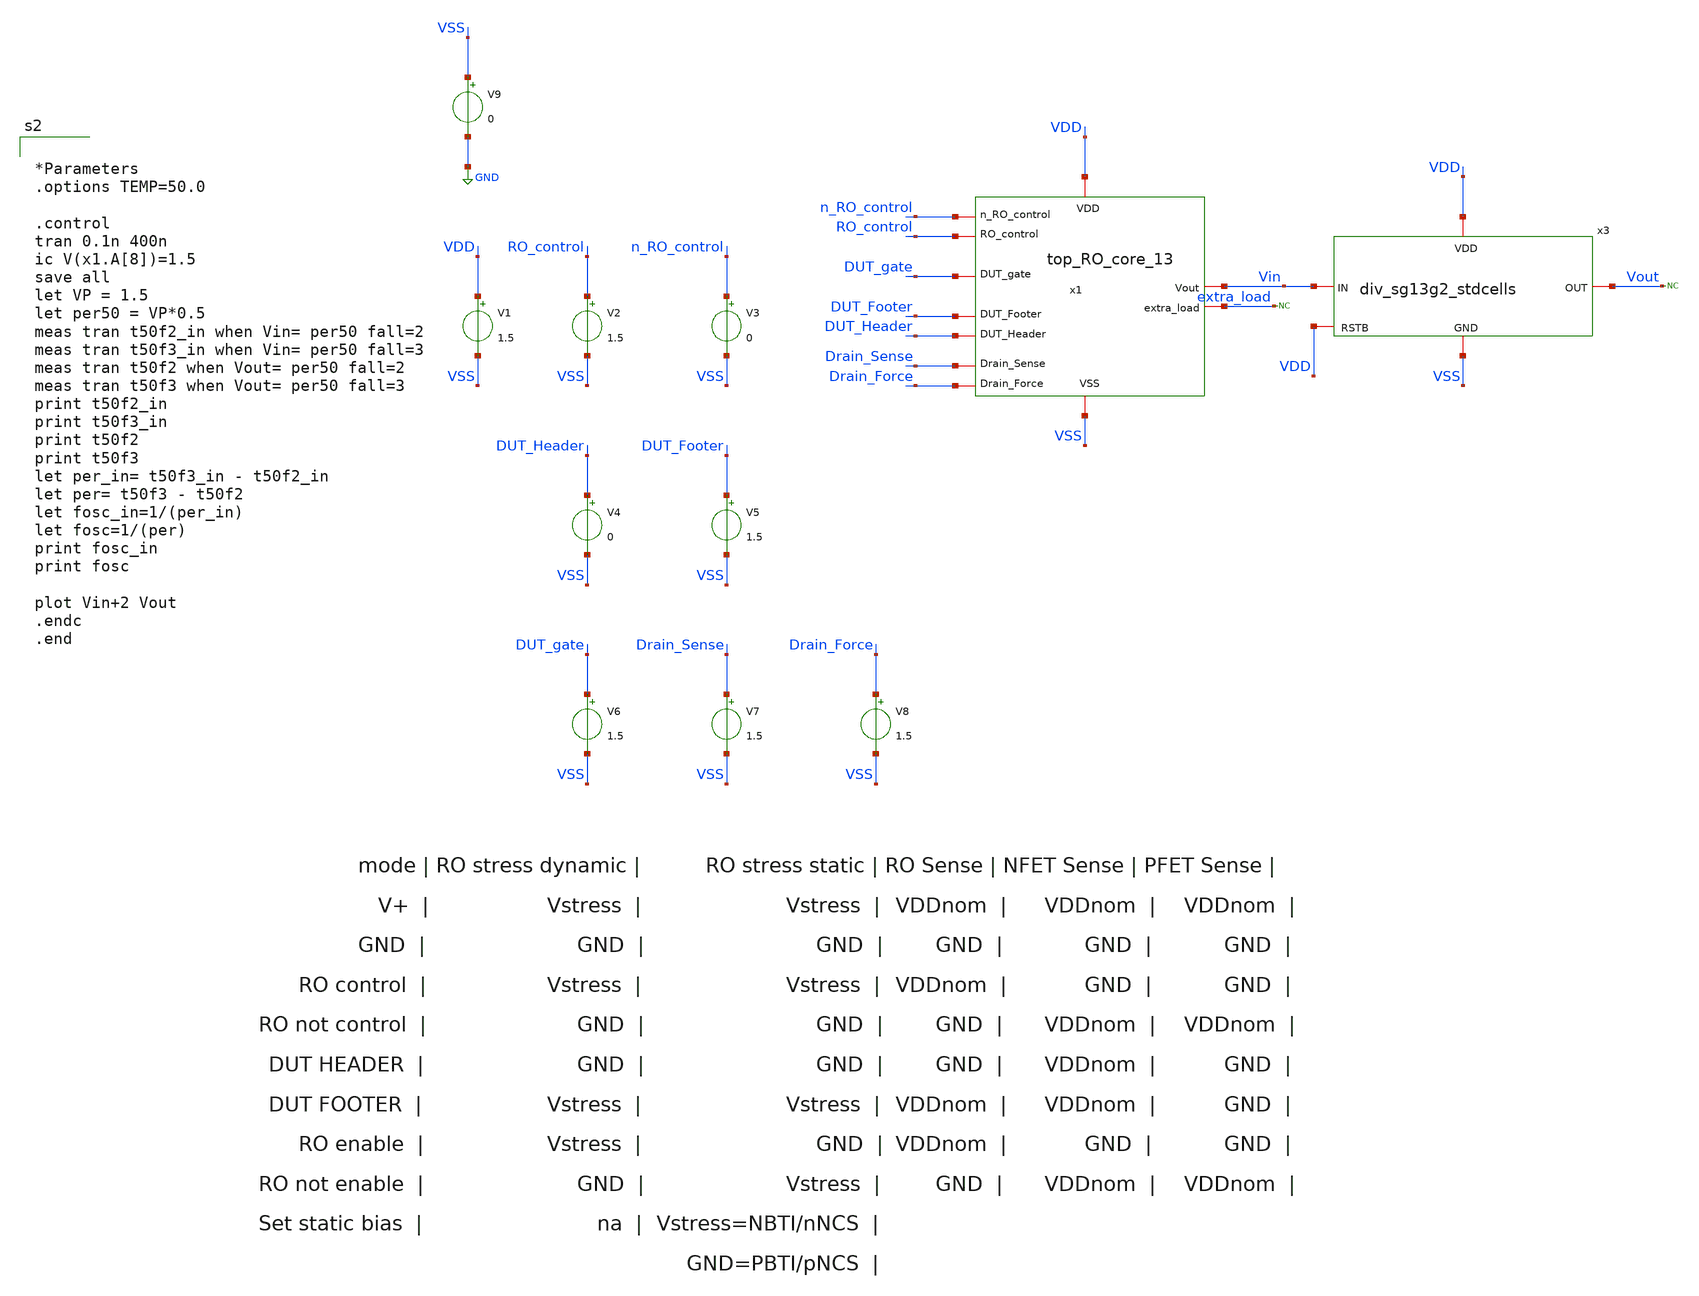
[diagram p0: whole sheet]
** sch_path: unic_cass_wrapper_user_project/ROs_reliability/top_RO_core_13_tb.sch
**.subckt top_RO_core_13_tb
V1 VDD VSS 1.5
V2 RO_control VSS 1.5
V3 n_RO_control VSS 0
V4 DUT_Header VSS 0
V5 DUT_Footer VSS 1.5
* noconn extra_load
* noconn Vout
x1 VDD VSS n_RO_control RO_control DUT_gate Vin DUT_Header DUT_Footer Drain_Force Drain_Sense
+ extra_load top_RO_core_13
V6 DUT_gate VSS 1.5
V7 Drain_Sense VSS 1.5
V8 Drain_Force VSS 1.5
V9 VSS GND 0
x3 VDD Vout Vin VSS VDD div_sg13g2_stdcells
**** begin user architecture code


*Parameters
.options TEMP=50.0

.control
tran 0.1n 400n
ic V(x1.A[8])=1.5
save all
let VP = 1.5
let per50 = VP*0.5
meas tran t50f2_in when Vin= per50 fall=2
meas tran t50f3_in when Vin= per50 fall=3
meas tran t50f2 when Vout= per50 fall=2
meas tran t50f3 when Vout= per50 fall=3
print t50f2_in
print t50f3_in
print t50f2
print t50f3
let per_in= t50f3_in - t50f2_in
let per= t50f3 - t50f2
let fosc_in=1/(per_in)
let fosc=1/(per)
print fosc_in
print fosc

plot Vin+2 Vout
.endc
.end


 .lib cornerMOSlv.lib mos_tt
.include sg13g2_stdcell.spice
.include /home/jsmoya07/Documents/asicone_sg13g2/lib/sg13g2.ckt

**** end user architecture code
**.ends

* expanding   symbol:  top_RO_core_13.sym # of pins=11
** sym_path: unic_cass_wrapper_user_project/ROs_reliability/top_RO_core_13.sym
** sch_path: unic_cass_wrapper_user_project/ROs_reliability/top_RO_core_13.sch
.subckt top_RO_core_13 VDD VSS n_RO_control RO_control DUT_gate Vout DUT_Header DUT_Footer
+ Drain_Force Drain_Sense extra_load
*.iopin VDD
*.iopin VSS
*.iopin n_RO_control
*.iopin RO_control
*.iopin DUT_gate
*.iopin extra_load
*.iopin DUT_Header
*.iopin DUT_Footer
*.iopin Drain_Force
*.iopin Drain_Sense
*.iopin Vout
x1 VDD VSS A[9] A[8] rovcel2
x7 VDD VSS A[9] n_RO_control A_10 RO_control DUT_gate rovcel3
x2 DUT_Header DUT_Footer Drain_Force Drain_Sense RO_control n_RO_control VDD VSS A_10 extra_load
+ rovcel1
x3 VDD VSS extra_load n_RO_control A_12 rovcel4
x4 VDD VSS Vout A_12 rovcel2
x5[1] VDD VSS A[8] A[7] rovcel2
x5[2] VDD VSS A[7] A[6] rovcel2
x5[3] VDD VSS A[6] A[5] rovcel2
x5[4] VDD VSS A[5] A[4] rovcel2
x5[5] VDD VSS A[4] A[3] rovcel2
x5[6] VDD VSS A[3] A[2] rovcel2
x5[7] VDD VSS A[2] A[1] rovcel2
x5[8] VDD VSS A[1] Vout rovcel2
.ends


* expanding   symbol:  /home/jsmoya07/Documents/RO_reliability/xschem/div_sg13g2_stdcells.sym # of
*+ pins=5
** sym_path: unic_cass_wrapper_user_project/ROs_reliability/div_sg13g2_stdcells.sym
** sch_path: unic_cass_wrapper_user_project/ROs_reliability/div_sg13g2_stdcells.sch
.subckt div_sg13g2_stdcells VDD OUT IN GND RSTB
*.iopin GND
*.iopin IN
*.iopin VDD
*.iopin OUT
*.iopin RSTB
x2 q2 qn2 q1 qn2 RSTB VDD GND sg13g2_dfrbp_1
x1 q1 qn1 IN qn1 RSTB VDD GND sg13g2_dfrbp_1
x3 q3 qn3 q2 qn3 RSTB VDD GND sg13g2_dfrbp_1
x4 q4 qn4 q3 qn4 RSTB VDD GND sg13g2_dfrbp_1
x5 OUT qn5 q4 qn5 RSTB VDD GND sg13g2_dfrbp_1
.ends


* expanding   symbol:  rovcel2.sym # of pins=4
** sym_path: rovcel2.sym
** sch_path: rovcel2.sch
.subckt rovcel2 VDD VSS Vout Vin
*.iopin VDD
*.iopin VSS
*.iopin Vin
*.iopin Vout
* noconn #net1
* noconn #net2
x5 VDD Vin Vout VSS inverter_RO_rel
x1 VDD VDD Vout net2 VSS VSS tgate
x3 VDD VDD Vout net1 VSS VSS tgate
.ends


* expanding   symbol:  rovcel3.sym # of pins=7
** sym_path: rovcel3.sym
** sch_path: rovcel3.sch
.subckt rovcel3 VDD VSS Vin n_RO_control Vout RO_control DUT_gate
*.iopin VDD
*.iopin VSS
*.iopin Vin
*.iopin n_RO_control
*.iopin RO_control
*.iopin DUT_gate
*.iopin Vout
* noconn #net1
x4 VDD VSS Vin n_RO_control RO_control Vout tristate_inv
x1 RO_control VDD Vout net1 VSS n_RO_control tgate
x5 RO_control VDD Vout DUT_gate VSS n_RO_control tgate
.ends


* expanding   symbol:  rovcel1.sym # of pins=10
** sym_path: rovcel1.sym
** sch_path: rovcel1.sch
.subckt rovcel1 DUT_Header DUT_Footer Drain_Force Drain_Sense RO_control n_RO_control VDD VSS Vin
+ Vout
*.iopin VDD
*.iopin VSS
*.iopin Vin
*.iopin DUT_Header
*.iopin DUT_Footer
*.iopin Drain_Force
*.iopin Vout
*.iopin Drain_Sense
*.iopin RO_control
*.iopin n_RO_control
x4 VDD VSS Vin DUT_Header DUT_Footer Vout tristate_inv
x1 RO_control VDD Vout Drain_Force VSS n_RO_control tgate_force
x3 RO_control VDD Vout Drain_Sense VSS n_RO_control tgate
.ends


* expanding   symbol:  rovcel4.sym # of pins=5
** sym_path: rovcel4.sym
** sch_path: rovcel4.sch
.subckt rovcel4 VDD VSS Vin n_RO_control Vout
*.iopin VDD
*.iopin VSS
*.iopin Vin
*.iopin n_RO_control
*.iopin Vout
* noconn #net1
x4 n_RO_control VDD VSS Vin Vout inv1
x1 VDD VDD Vout VSS VSS VSS tgate
x5 VDD VDD Vout net1 VSS VSS tgate
.ends


* expanding   symbol:  sg13g2_stdcells/sg13g2_dfrbp_1.sym # of pins=5
** sym_path: sg13g2_stdcells/sg13g2_dfrbp_1.sym
** sch_path: sg13g2_stdcells/sg13g2_dfrbp_1.sch
.subckt sg13g2_dfrbp_1 Q Q_N CLK D RESET_B VDD VSS
*.ipin D
*.ipin RESET_B
*.ipin CLK
*.opin Q
*.opin Q_N
*.iopin VDD
*.iopin VSS
XM1 Db D net10 VSS sg13_lv_nmos w=420.00n l=130.00n ng=1 m=1 mm_ok=1
XM2 net10 RESET_B VSS VSS sg13_lv_nmos w=420.00n l=130.00n ng=1 m=1 mm_ok=1
XM3 net1 clkneg net9 VSS sg13_lv_nmos w=420.00n l=130.00n ng=1 m=1 mm_ok=1
XM4 net9 net1 VSS VSS sg13_lv_nmos w=420.00n l=130.00n ng=1 m=1 mm_ok=1
XM5 net1 net1 net5 VSS sg13_lv_nmos w=420.00n l=130.00n ng=1 m=1 mm_ok=1
XM6 net5 RESET_B VSS VSS sg13_lv_nmos w=420.00n l=130.00n ng=1 m=1 mm_ok=1
XM7 Q_N net1 VSS VSS sg13_lv_nmos w=740.00n l=130.00n ng=1 m=1 mm_ok=1
XM8 net2 net1 VSS VSS sg13_lv_nmos w=740.00n l=130.00n ng=1 m=1 mm_ok=1
XM9 Q net2 VSS VSS sg13_lv_nmos w=740.00n l=130.00n ng=1 m=1 mm_ok=1
XM10 clkneg CLK VSS VSS sg13_lv_nmos w=740.00n l=130.00n ng=1 m=1 mm_ok=1
XM11 clkpos clkneg VSS VSS sg13_lv_nmos w=740.00n l=130.00n ng=1 m=1 mm_ok=1
XM12 Db clkneg net3 VSS sg13_lv_nmos w=420.00n l=130.00n ng=1 m=1 mm_ok=1
XM13 net3 clkpos net8 VSS sg13_lv_nmos w=420.00n l=130.00n ng=1 m=1 mm_ok=1
XM14 net8 net3 net4 VSS sg13_lv_nmos w=420.00n l=130.00n ng=1 m=1 mm_ok=1
XM15 net4 RESET_B VSS VSS sg13_lv_nmos w=420.00n l=130.00n ng=1 m=1 mm_ok=1
XM16 net3 net3 VSS VSS sg13_lv_nmos w=740.00n l=130.00n ng=1 m=1 mm_ok=1
XM17 net3 clkpos net1 VSS sg13_lv_nmos w=740.00n l=130.00n ng=1 m=1 mm_ok=1
XM18 Db RESET_B VDD VDD sg13_lv_pmos w=420.00n l=130.00n ng=1 m=1 mm_ok=1
XM19 Db D VDD VDD sg13_lv_pmos w=420.00n l=130.00n ng=1 m=1 mm_ok=1
XM20 net7 net1 VDD VDD sg13_lv_pmos w=420.00n l=130.00n ng=1 m=1 mm_ok=1
XM21 net1 clkpos net7 VDD sg13_lv_pmos w=420.00n l=130.00n ng=1 m=1 mm_ok=1
XM22 net1 net1 VDD VDD sg13_lv_pmos w=420.00n l=130.00n ng=1 m=1 mm_ok=1
XM23 net1 RESET_B VDD VDD sg13_lv_pmos w=420.00n l=130.00n ng=1 m=1 mm_ok=1
XM24 Q_N net1 VDD VDD sg13_lv_pmos w=1.12u l=130.00n ng=1 m=1 mm_ok=1
XM25 net2 net1 VDD VDD sg13_lv_pmos w=1.12u l=130.00n ng=1 m=1 mm_ok=1
XM26 Q net2 VDD VDD sg13_lv_pmos w=1.12u l=130.00n ng=1 m=1 mm_ok=1
XM27 clkneg CLK VDD VDD sg13_lv_pmos w=1.12u l=130.00n ng=1 m=1 mm_ok=1
XM28 clkpos clkneg VDD VDD sg13_lv_pmos w=1.12u l=130.00n ng=1 m=1 mm_ok=1
XM29 Db clkpos net3 VDD sg13_lv_pmos w=420.00n l=130.00n ng=1 m=1 mm_ok=1
XM30 net6 net3 VDD VDD sg13_lv_pmos w=420.00n l=130.00n ng=1 m=1 mm_ok=1
XM31 net3 clkneg net6 VDD sg13_lv_pmos w=420.00n l=130.00n ng=1 m=1 mm_ok=1
XM32 net3 RESET_B VDD VDD sg13_lv_pmos w=420.00n l=130.00n ng=1 m=1 mm_ok=1
XM33 net3 net3 VDD VDD sg13_lv_pmos w=1.000u l=130.00n ng=1 m=1 mm_ok=1
XM34 net3 clkneg net1 VDD sg13_lv_pmos w=1.000u l=130.00n ng=1 m=1 mm_ok=1
.ends


* expanding   symbol:  inverter_RO_rel.sym # of pins=4
** sym_path: inverter_RO_rel.sym
** sch_path: inverter_RO_rel.sch
.subckt inverter_RO_rel VDD Vin Vout VSS
*.iopin VDD
*.iopin VSS
*.iopin Vin
*.iopin Vout
XM3 Vout Vin VDD VDD sg13_lv_pmos w=3.4u l=0.45u ng=1 m=4 mm_ok=1
XM1 VSS Vin Vout VSS sg13_lv_nmos w=1.3u l=0.45u ng=1 m=4 mm_ok=1
.ends


* expanding   symbol:  tgate.sym # of pins=6
** sym_path: tgate.sym
** sch_path: tgate.sch
.subckt tgate nclk VDD Vin Vout VSS clk
*.iopin nclk
*.iopin clk
*.iopin VDD
*.iopin VSS
*.iopin Vout
*.iopin Vin
XM3 Vout nclk Vin VDD sg13_lv_pmos w=3.4u l=0.45u ng=1 m=1 mm_ok=1
XM1 Vout clk Vin VSS sg13_lv_nmos w=1.3u l=0.45u ng=1 m=1 mm_ok=1
.ends


* expanding   symbol:  tristate_inv.sym # of pins=6
** sym_path: tristate_inv.sym
** sch_path: tristate_inv.sch
.subckt tristate_inv VDD VSS Vin Vup Vdn Vout
*.iopin VDD
*.iopin VSS
*.iopin Vin
*.iopin Vout
*.iopin Vup
*.iopin Vdn
XM5 Vout Vin net1 VDD sg13_lv_pmos w=3.4u l=0.45u ng=1 m=4 mm_ok=1
XM2 net2 Vin Vout VSS sg13_lv_nmos w=1.3u l=0.45u ng=1 m=4 mm_ok=1
XM1 net1 Vup VDD VDD sg13_lv_pmos w=3.4u l=0.45u ng=1 m=12 mm_ok=1
XM3 VSS Vdn net2 VSS sg13_lv_nmos w=1.3u l=0.45u ng=1 m=12 mm_ok=1
.ends


* expanding   symbol:  tgate_force.sym # of pins=6
** sym_path: tgate_force.sym
** sch_path: tgate_force.sch
.subckt tgate_force nclk VDD Vin Vout VSS clk
*.iopin nclk
*.iopin clk
*.iopin VDD
*.iopin VSS
*.iopin Vout
*.iopin Vin
XM3 Vout nclk Vin VDD sg13_lv_pmos w=3.4u l=0.45u ng=1 m=4 mm_ok=1
XM4 Vout clk Vin VSS sg13_lv_nmos w=1.3u l=0.45u ng=1 m=4 mm_ok=1
.ends


* expanding   symbol:  inv1.sym # of pins=5
** sym_path: inv1.sym
** sch_path: inv1.sch
.subckt inv1 n_RO_control VDD VSS Vin Vout
*.iopin VDD
*.iopin VSS
*.iopin Vin
*.iopin Vout
*.iopin n_RO_control
XM1 net1 n_RO_control VDD VDD sg13_lv_pmos w=3.4u l=0.45u ng=1 m=12 mm_ok=1
XM5 Vout Vin net1 VDD sg13_lv_pmos w=3.4u l=0.45u ng=1 m=4 mm_ok=1
XM2 VSS Vin Vout VSS sg13_lv_nmos w=1.3u l=0.45u ng=1 m=4 mm_ok=1
.ends

.GLOBAL GND
.end
